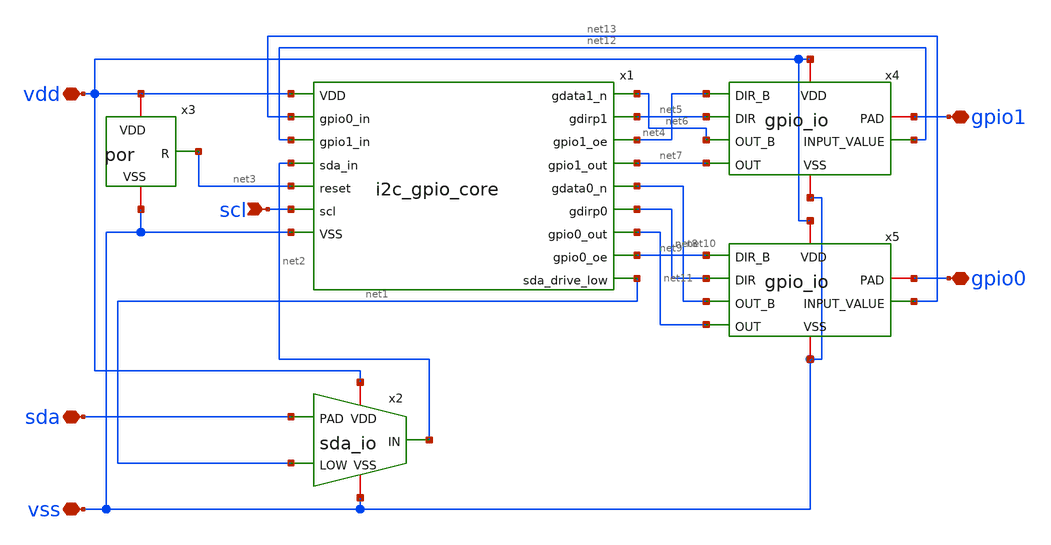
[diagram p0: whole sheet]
** sch_path: examples/i2c_gpio_2bit/reference/manual_layout_122/i2c_gpio_fullchip.sch
**.subckt i2c_gpio_fullchip vdd vss sda scl gpio1 gpio0
*.iopin vdd
*.iopin vss
*.iopin sda
*.ipin scl
*.iopin gpio1
*.iopin gpio0
x1 net13 net12 net3 scl net2 net10 net6 net8 net5 net9 net11 net4 net7 net1 vdd vss i2c_gpio_core
x2 vdd sda net2 net1 vss sda_io
x3 vdd net3 vss por
x4 vdd net4 net5 net6 net7 gpio1 net12 vss gpio_io
x5 vdd net9 net8 net10 net11 gpio0 net13 vss gpio_io
**.ends
.end
